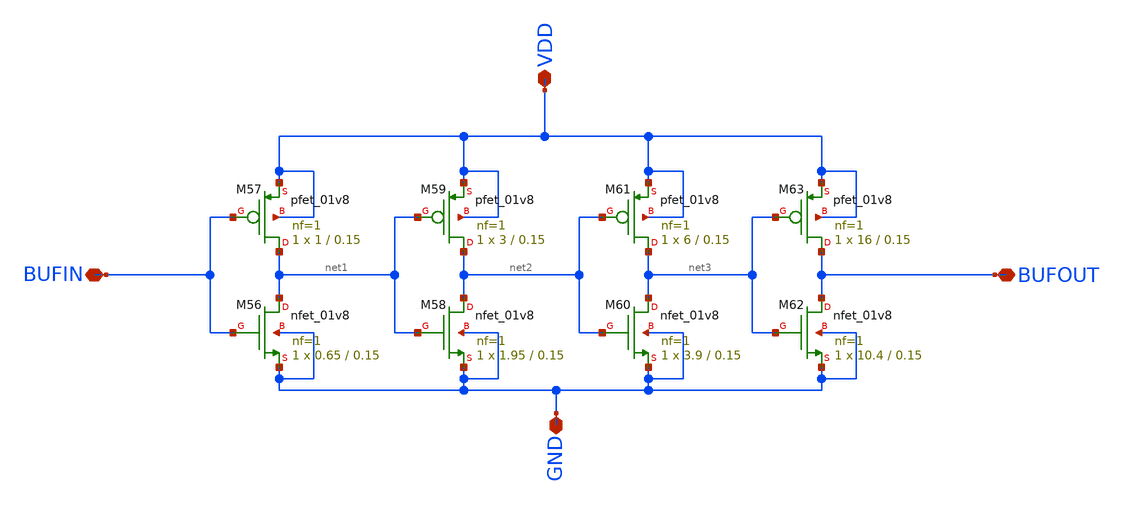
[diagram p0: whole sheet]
** sch_path: xschem/buffer.sch
**.subckt buffer BUFIN BUFOUT VDD GND
*.iopin BUFIN
*.iopin BUFOUT
*.iopin VDD
*.iopin GND
XM56 net1 BUFIN GND GND sky130_fd_pr__nfet_01v8 L=0.15 W=0.65 nf=1 ad='int((nf+1)/2) * W/nf * 0.29' as='int((nf+2)/2) * W/nf * 0.29'
+ pd='2*int((nf+1)/2) * (W/nf + 0.29)' ps='2*int((nf+2)/2) * (W/nf + 0.29)' nrd='0.29 / W' nrs='0.29 / W'
+ sa=0 sb=0 sd=0 mult=1 m=1
XM57 net1 BUFIN VDD VDD sky130_fd_pr__pfet_01v8 L=0.15 W=1 nf=1 ad='int((nf+1)/2) * W/nf * 0.29' as='int((nf+2)/2) * W/nf * 0.29'
+ pd='2*int((nf+1)/2) * (W/nf + 0.29)' ps='2*int((nf+2)/2) * (W/nf + 0.29)' nrd='0.29 / W' nrs='0.29 / W'
+ sa=0 sb=0 sd=0 mult=1 m=1
XM58 net2 net1 GND GND sky130_fd_pr__nfet_01v8 L=0.15 W=1.95 nf=1 ad='int((nf+1)/2) * W/nf * 0.29' as='int((nf+2)/2) * W/nf * 0.29'
+ pd='2*int((nf+1)/2) * (W/nf + 0.29)' ps='2*int((nf+2)/2) * (W/nf + 0.29)' nrd='0.29 / W' nrs='0.29 / W'
+ sa=0 sb=0 sd=0 mult=1 m=1
XM59 net2 net1 VDD VDD sky130_fd_pr__pfet_01v8 L=0.15 W=3 nf=1 ad='int((nf+1)/2) * W/nf * 0.29' as='int((nf+2)/2) * W/nf * 0.29'
+ pd='2*int((nf+1)/2) * (W/nf + 0.29)' ps='2*int((nf+2)/2) * (W/nf + 0.29)' nrd='0.29 / W' nrs='0.29 / W'
+ sa=0 sb=0 sd=0 mult=1 m=1
XM60 net3 net2 GND GND sky130_fd_pr__nfet_01v8 L=0.15 W=3.9 nf=1 ad='int((nf+1)/2) * W/nf * 0.29' as='int((nf+2)/2) * W/nf * 0.29'
+ pd='2*int((nf+1)/2) * (W/nf + 0.29)' ps='2*int((nf+2)/2) * (W/nf + 0.29)' nrd='0.29 / W' nrs='0.29 / W'
+ sa=0 sb=0 sd=0 mult=1 m=1
XM61 net3 net2 VDD VDD sky130_fd_pr__pfet_01v8 L=0.15 W=6 nf=1 ad='int((nf+1)/2) * W/nf * 0.29' as='int((nf+2)/2) * W/nf * 0.29'
+ pd='2*int((nf+1)/2) * (W/nf + 0.29)' ps='2*int((nf+2)/2) * (W/nf + 0.29)' nrd='0.29 / W' nrs='0.29 / W'
+ sa=0 sb=0 sd=0 mult=1 m=1
XM62 BUFOUT net3 GND GND sky130_fd_pr__nfet_01v8 L=0.15 W=10.4 nf=1 ad='int((nf+1)/2) * W/nf * 0.29'
+ as='int((nf+2)/2) * W/nf * 0.29' pd='2*int((nf+1)/2) * (W/nf + 0.29)' ps='2*int((nf+2)/2) * (W/nf + 0.29)'
+ nrd='0.29 / W' nrs='0.29 / W' sa=0 sb=0 sd=0 mult=1 m=1
XM63 BUFOUT net3 VDD VDD sky130_fd_pr__pfet_01v8 L=0.15 W=16 nf=1 ad='int((nf+1)/2) * W/nf * 0.29' as='int((nf+2)/2) * W/nf * 0.29'
+ pd='2*int((nf+1)/2) * (W/nf + 0.29)' ps='2*int((nf+2)/2) * (W/nf + 0.29)' nrd='0.29 / W' nrs='0.29 / W'
+ sa=0 sb=0 sd=0 mult=1 m=1
**.ends
.end
